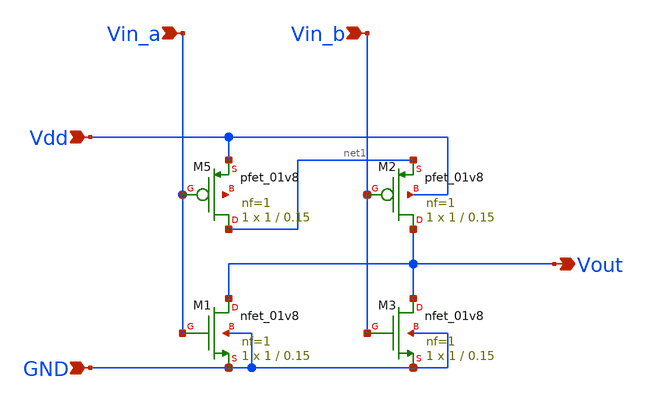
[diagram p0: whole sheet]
** sch_path: NOR.sch
**.subckt NOR Vout Vdd GND Vin_a Vin_b
*.opin Vout
*.ipin Vdd
*.ipin GND
*.ipin Vin_a
*.ipin Vin_b
XM1 Vout Vin_a GND GND sky130_fd_pr__nfet_01v8 L=0.15 W=1 nf=1 ad='int((1 + 1)/2) * 1 / 1 * 0.29' as='int((1 + 2)/2) * 1 / 1 * 0.29'
+ pd='2*int((1 + 1)/2) * (1 / 1 + 0.29)' ps='2*int((1 + 2)/2) * (1 / 1 + 0.29)' nrd='0.29 / 1 ' nrs='0.29 / 1 '
+ sa=0 sb=0 sd=0 mult=1 m=1
XM3 Vout Vin_b GND GND sky130_fd_pr__nfet_01v8 L=0.15 W=1 nf=1 ad='int((1 + 1)/2) * 1 / 1 * 0.29' as='int((1 + 2)/2) * 1 / 1 * 0.29'
+ pd='2*int((1 + 1)/2) * (1 / 1 + 0.29)' ps='2*int((1 + 2)/2) * (1 / 1 + 0.29)' nrd='0.29 / 1 ' nrs='0.29 / 1 '
+ sa=0 sb=0 sd=0 mult=1 m=1
XM5 net1 Vin_a Vdd net2 sky130_fd_pr__pfet_01v8 L=0.15 W=1 nf=1 ad='int((1 + 1)/2) * 1 / 1 * 0.29' as='int((1 + 2)/2) * 1 / 1 * 0.29'
+ pd='2*int((1 + 1)/2) * (1 / 1 + 0.29)' ps='2*int((1 + 2)/2) * (1 / 1 + 0.29)' nrd='0.29 / 1 ' nrs='0.29 / 1 '
+ sa=0 sb=0 sd=0 mult=1 m=1
XM2 Vout Vin_b net1 Vdd sky130_fd_pr__pfet_01v8 L=0.15 W=1 nf=1 ad='int((1 + 1)/2) * 1 / 1 * 0.29' as='int((1 + 2)/2) * 1 / 1 * 0.29'
+ pd='2*int((1 + 1)/2) * (1 / 1 + 0.29)' ps='2*int((1 + 2)/2) * (1 / 1 + 0.29)' nrd='0.29 / 1 ' nrs='0.29 / 1 '
+ sa=0 sb=0 sd=0 mult=1 m=1
**.ends
.end
